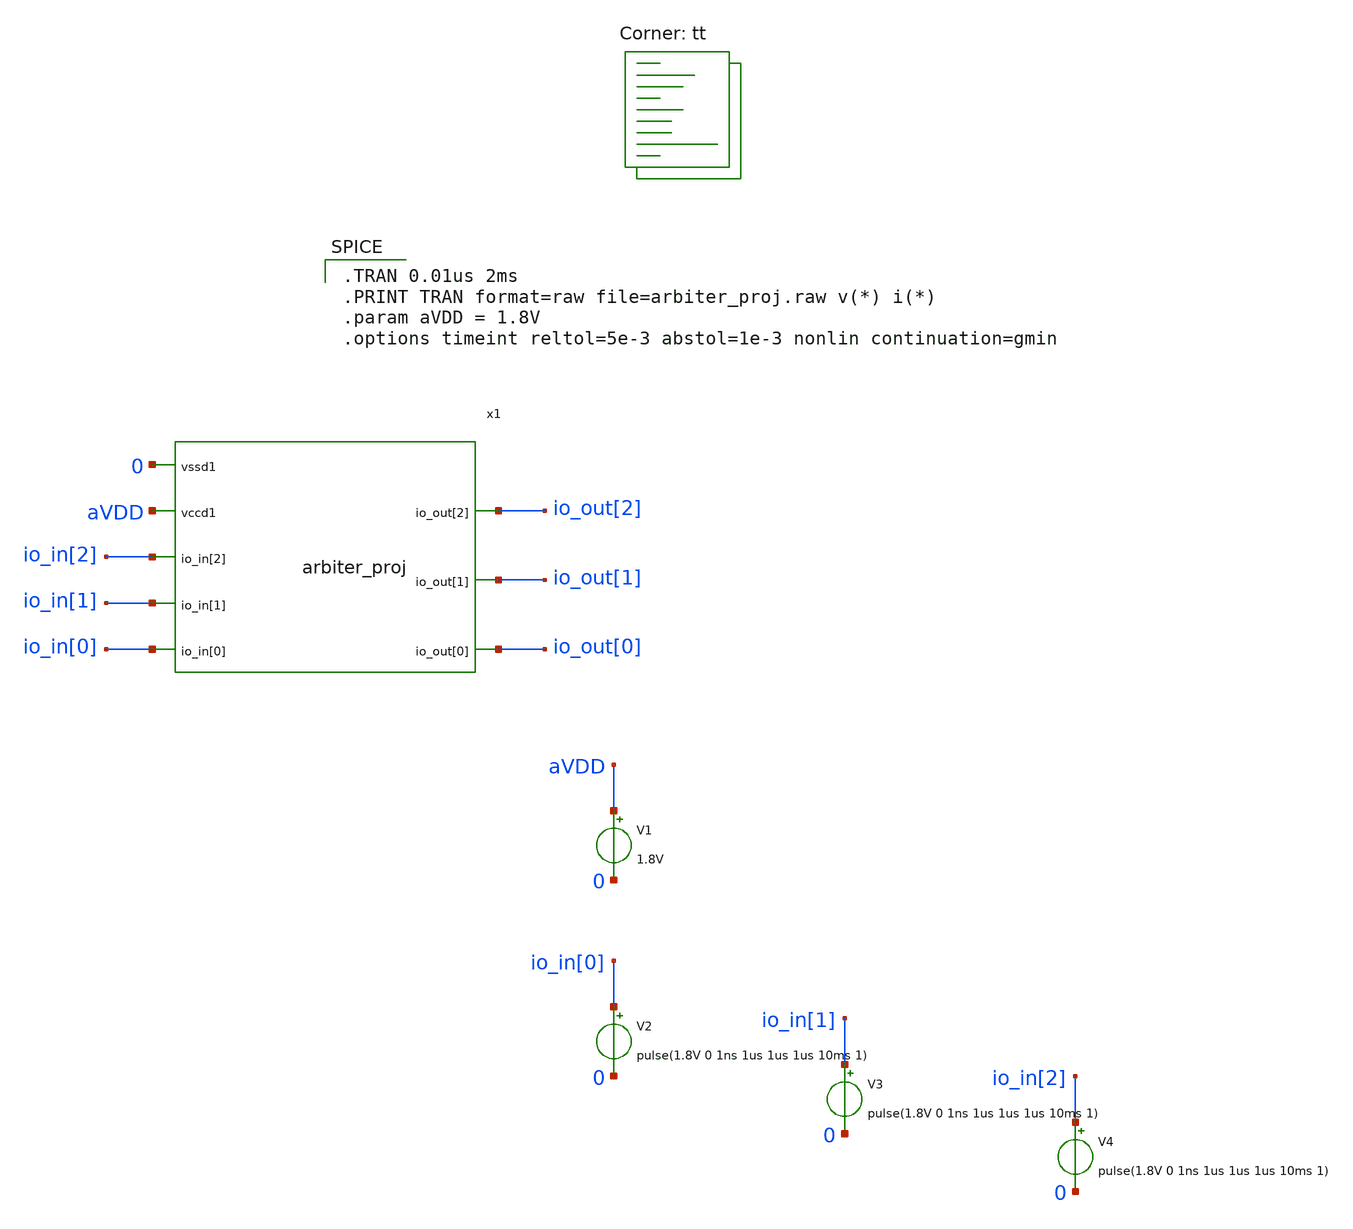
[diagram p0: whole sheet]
** sch_path: xschem/arbiter_proj_tb.sch
**.subckt arbiter_proj_tb
V1 aVDD 0 1.8V
x1 io_in[0] io_in[1] io_in[2] io_out[0] io_out[1] io_out[2] aVDD 0 arbiter_proj
V2 io_in[0] 0 pulse(1.8V 0 1ns 1us 1us 1us 10ms 1)
V3 io_in[1] 0 pulse(1.8V 0 1ns 1us 1us 1us 10ms 1)
V4 io_in[2] 0 pulse(1.8V 0 1ns 1us 1us 1us 10ms 1)
**** begin user architecture code

.TRAN 0.01us 2ms
.PRINT TRAN format=raw file=arbiter_proj.raw v(*) i(*)
.param aVDD = 1.8V
.options timeint reltol=5e-3 abstol=1e-3 nonlin continuation=gmin



.include $::SKYWATER_STDCELLS/sky130_fd_sc_hd.spice

.lib $::SKYWATER_MODELS/sky130.lib.spice tt
**** end user architecture code
**.ends

* expanding   symbol:  /home/vasilis/Internship/dedicated_async/xschem/arbiter_proj.sym # of pins=8
** sym_path: xschem/arbiter_proj.sym
.include /home/vasilis/Internship/dedicated_async/spi/lvs/arbiter_proj.spice
.end
